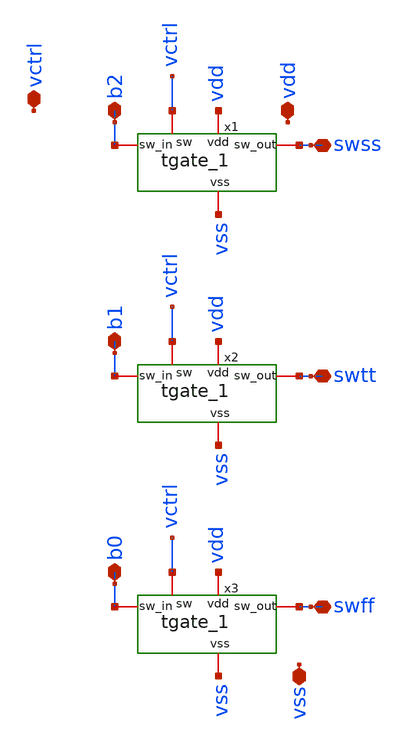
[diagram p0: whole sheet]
** sch_path: xschem/stf_ctrl.sch
**.subckt stf_ctrl vctrl vdd vss b0 b1 b2 swss swtt swff
*.iopin vctrl
*.iopin vdd
*.iopin vss
*.iopin b0
*.iopin b1
*.iopin b2
*.iopin swss
*.iopin swtt
*.iopin swff
x1 swss b2 vss vdd vctrl tgate_1
x2 swtt b1 vss vdd vctrl tgate_1
x3 swff b0 vss vdd vctrl tgate_1
**.ends

* expanding   symbol:  tgate_1.sym # of pins=5
** sym_path: xschem/tgate_1.sym
** sch_path: xschem/tgate_1.sch
.subckt tgate_1 sw_out sw_in vss vdd sw
*.iopin sw_in
*.iopin vdd
*.iopin vss
*.iopin sw
*.iopin sw_out
XM17 sw_out sw sw_in vdd sky130_fd_pr__pfet_01v8 L=0.15 W=1.4 nf=2 ad='int((nf+1)/2) * W/nf * 0.29' as='int((nf+2)/2) * W/nf * 0.29'
+ pd='2*int((nf+1)/2) * (W/nf + 0.29)' ps='2*int((nf+2)/2) * (W/nf + 0.29)' nrd='0.29 / W' nrs='0.29 / W'
+ sa=0 sb=0 sd=0 mult=1 m=1
XM18 sw_in net1 sw_out vss sky130_fd_pr__nfet_01v8 L=0.15 W=1.4 nf=2 ad='int((nf+1)/2) * W/nf * 0.29'
+ as='int((nf+2)/2) * W/nf * 0.29' pd='2*int((nf+1)/2) * (W/nf + 0.29)' ps='2*int((nf+2)/2) * (W/nf + 0.29)'
+ nrd='0.29 / W' nrs='0.29 / W' sa=0 sb=0 sd=0 mult=1 m=1
x1 vdd sw net1 vss inv_simple1
XM1 sw_out sw_out sw_out vdd sky130_fd_pr__pfet_01v8 L=0.15 W=1.4 nf=2 ad='int((nf+1)/2) * W/nf * 0.29'
+ as='int((nf+2)/2) * W/nf * 0.29' pd='2*int((nf+1)/2) * (W/nf + 0.29)' ps='2*int((nf+2)/2) * (W/nf + 0.29)'
+ nrd='0.29 / W' nrs='0.29 / W' sa=0 sb=0 sd=0 mult=1 m=1
XM2 sw_out sw_out sw_out vss sky130_fd_pr__nfet_01v8 L=0.15 W=1.4 nf=2 ad='int((nf+1)/2) * W/nf * 0.29'
+ as='int((nf+2)/2) * W/nf * 0.29' pd='2*int((nf+1)/2) * (W/nf + 0.29)' ps='2*int((nf+2)/2) * (W/nf + 0.29)'
+ nrd='0.29 / W' nrs='0.29 / W' sa=0 sb=0 sd=0 mult=1 m=1
.ends


* expanding   symbol:  inv_simple1.sym # of pins=4
** sym_path: xschem/inv_simple1.sym
** sch_path: xschem/inv_simple1.sch
.subckt inv_simple1 vdd in out vss
*.iopin in
*.iopin vdd
*.iopin vss
*.iopin out
XM19 out in vss vss sky130_fd_pr__nfet_01v8 L=0.15 W=1.4 nf=1 ad='int((nf+1)/2) * W/nf * 0.29' as='int((nf+2)/2) * W/nf * 0.29'
+ pd='2*int((nf+1)/2) * (W/nf + 0.29)' ps='2*int((nf+2)/2) * (W/nf + 0.29)' nrd='0.29 / W' nrs='0.29 / W'
+ sa=0 sb=0 sd=0 mult=1 m=1
XM20 out in vdd vdd sky130_fd_pr__pfet_01v8 L=0.15 W=2.8 nf=1 ad='int((nf+1)/2) * W/nf * 0.29' as='int((nf+2)/2) * W/nf * 0.29'
+ pd='2*int((nf+1)/2) * (W/nf + 0.29)' ps='2*int((nf+2)/2) * (W/nf + 0.29)' nrd='0.29 / W' nrs='0.29 / W'
+ sa=0 sb=0 sd=0 mult=1 m=1
XM1 vdd vdd vdd vdd sky130_fd_pr__pfet_01v8 L=0.15 W=1.4 nf=1 ad='int((nf+1)/2) * W/nf * 0.29' as='int((nf+2)/2) * W/nf * 0.29'
+ pd='2*int((nf+1)/2) * (W/nf + 0.29)' ps='2*int((nf+2)/2) * (W/nf + 0.29)' nrd='0.29 / W' nrs='0.29 / W'
+ sa=0 sb=0 sd=0 mult=1 m=1
XM2 vss vss vss vss sky130_fd_pr__nfet_01v8 L=0.15 W=1.4 nf=1 ad='int((nf+1)/2) * W/nf * 0.29' as='int((nf+2)/2) * W/nf * 0.29'
+ pd='2*int((nf+1)/2) * (W/nf + 0.29)' ps='2*int((nf+2)/2) * (W/nf + 0.29)' nrd='0.29 / W' nrs='0.29 / W'
+ sa=0 sb=0 sd=0 mult=1 m=1
.ends

.end
